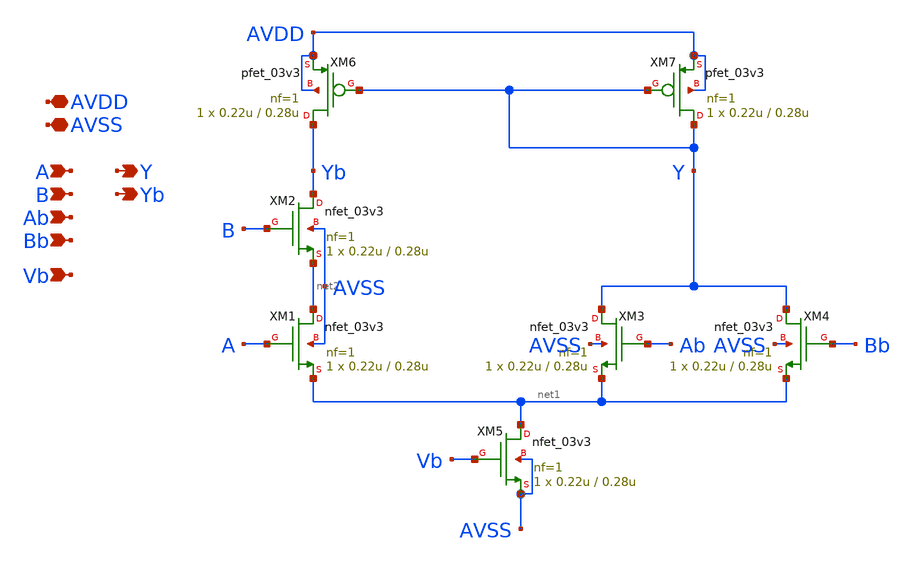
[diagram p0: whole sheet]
** sch_path: designs/libs/core_analog/cml_nand2/cml_nand2.sch
**.subckt cml_nand2 A B Ab Bb AVDD AVSS Vb Y Yb
*.ipin A
*.ipin B
*.ipin Ab
*.ipin Bb
*.iopin AVDD
*.iopin AVSS
*.ipin Vb
*.opin Y
*.opin Yb
XM1 net2 A net1 AVSS nfet_03v3 L=0.28u W=0.22u nf=1 ad='int((nf+1)/2) * W/nf * 0.18u' as='int((nf+2)/2) * W/nf * 0.18u'
+ pd='2*int((nf+1)/2) * (W/nf + 0.18u)' ps='2*int((nf+2)/2) * (W/nf + 0.18u)' nrd='0.18u / W' nrs='0.18u / W'
+ sa=0 sb=0 sd=0 m=1
XM2 Yb B net2 AVSS nfet_03v3 L=0.28u W=0.22u nf=1 ad='int((nf+1)/2) * W/nf * 0.18u' as='int((nf+2)/2) * W/nf * 0.18u'
+ pd='2*int((nf+1)/2) * (W/nf + 0.18u)' ps='2*int((nf+2)/2) * (W/nf + 0.18u)' nrd='0.18u / W' nrs='0.18u / W'
+ sa=0 sb=0 sd=0 m=1
XM3 Y Ab net1 AVSS nfet_03v3 L=0.28u W=0.22u nf=1 ad='int((nf+1)/2) * W/nf * 0.18u' as='int((nf+2)/2) * W/nf * 0.18u'
+ pd='2*int((nf+1)/2) * (W/nf + 0.18u)' ps='2*int((nf+2)/2) * (W/nf + 0.18u)' nrd='0.18u / W' nrs='0.18u / W'
+ sa=0 sb=0 sd=0 m=1
XM4 Y Bb net1 AVSS nfet_03v3 L=0.28u W=0.22u nf=1 ad='int((nf+1)/2) * W/nf * 0.18u' as='int((nf+2)/2) * W/nf * 0.18u'
+ pd='2*int((nf+1)/2) * (W/nf + 0.18u)' ps='2*int((nf+2)/2) * (W/nf + 0.18u)' nrd='0.18u / W' nrs='0.18u / W'
+ sa=0 sb=0 sd=0 m=1
XM5 net1 Vb AVSS AVSS nfet_03v3 L=0.28u W=0.22u nf=1 ad='int((nf+1)/2) * W/nf * 0.18u' as='int((nf+2)/2) * W/nf * 0.18u'
+ pd='2*int((nf+1)/2) * (W/nf + 0.18u)' ps='2*int((nf+2)/2) * (W/nf + 0.18u)' nrd='0.18u / W' nrs='0.18u / W'
+ sa=0 sb=0 sd=0 m=1
XM6 Yb Y AVDD AVDD pfet_03v3 L=0.28u W=0.22u nf=1 ad='int((nf+1)/2) * W/nf * 0.18u' as='int((nf+2)/2) * W/nf * 0.18u'
+ pd='2*int((nf+1)/2) * (W/nf + 0.18u)' ps='2*int((nf+2)/2) * (W/nf + 0.18u)' nrd='0.18u / W' nrs='0.18u / W'
+ sa=0 sb=0 sd=0 m=1
XM7 Y Y AVDD AVDD pfet_03v3 L=0.28u W=0.22u nf=1 ad='int((nf+1)/2) * W/nf * 0.18u' as='int((nf+2)/2) * W/nf * 0.18u'
+ pd='2*int((nf+1)/2) * (W/nf + 0.18u)' ps='2*int((nf+2)/2) * (W/nf + 0.18u)' nrd='0.18u / W' nrs='0.18u / W'
+ sa=0 sb=0 sd=0 m=1
**.ends
.end
